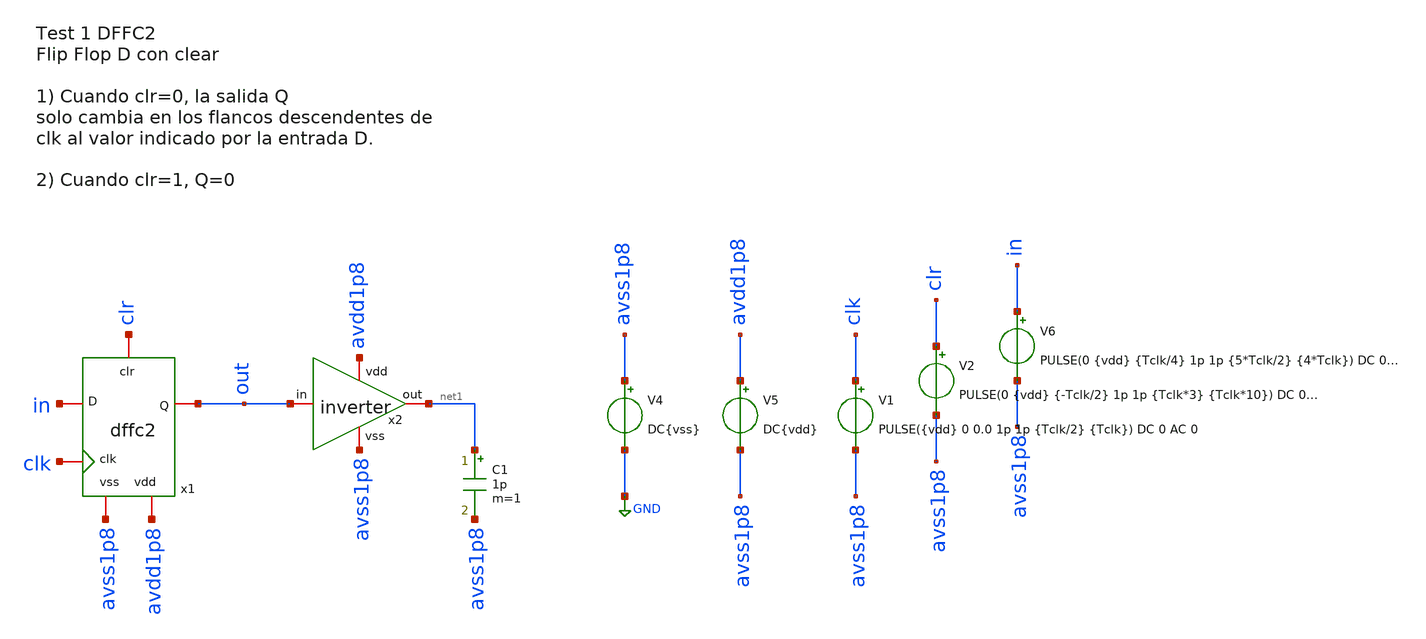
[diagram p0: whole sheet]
** sch_path: designs/sch/tests/test1_dffc2.sch
**.subckt test1_dffc2
x2 avdd1p8 net1 out avss1p8 inverter
V4 avss1p8 GND DC{vss}
V5 avdd1p8 avss1p8 DC{vdd}
V6 in avss1p8 PULSE(0 {vdd} {Tclk/4} 1p 1p {5*Tclk/2} {4*Tclk}) DC 0 AC 0
C1 net1 avss1p8 1p m=1
V1 clk avss1p8 PULSE({vdd} 0 0.0 1p 1p {Tclk/2} {Tclk}) DC 0 AC 0
V2 clr avss1p8 PULSE(0 {vdd} {-Tclk/2} 1p 1p {Tclk*3} {Tclk*10}) DC 0 AC 0
x1 out in clk clr avss1p8 avdd1p8 dffc2
**** begin user architecture code


* Circuit Parameters
.param vdd = 1.8
.param vss = 0.0
.param Tclk = 10n
.options TEMP = 65.0

* Include Models
.lib /foss/pdks/sky130A/libs.tech/ngspice/sky130.lib.spice TT

* OP Parameters & Singals to save
.save all

* Simulations
.control
  tran 0.01u 240n
  setplot tran1
  plot clr v(in)+2 v(out)+4 clk+6
reset
.endc

.end


**** end user architecture code
**.ends

* expanding   symbol:  /foss/designs/sch/inverter.sym # of pins=4
** sym_path: designs/inverter.sym
** sch_path: designs/inverter.sch
.subckt inverter vdd out in vss
*.iopin out
*.iopin vss
*.iopin vdd
*.iopin in
XM2 out in vss vss sky130_fd_pr__nfet_01v8 L=0.15 W=0.75 nf=1 ad='int((nf+1)/2) * W/nf * 0.29' as='int((nf+2)/2) * W/nf * 0.29'
+ pd='2*int((nf+1)/2) * (W/nf + 0.29)' ps='2*int((nf+2)/2) * (W/nf + 0.29)' nrd='0.29 / W' nrs='0.29 / W'
+ sa=0 sb=0 sd=0 mult=1 m=1
XM1 out in vdd vdd sky130_fd_pr__pfet_01v8 L=0.15 W=1.5 nf=1 ad='int((nf+1)/2) * W/nf * 0.29' as='int((nf+2)/2) * W/nf * 0.29'
+ pd='2*int((nf+1)/2) * (W/nf + 0.29)' ps='2*int((nf+2)/2) * (W/nf + 0.29)' nrd='0.29 / W' nrs='0.29 / W'
+ sa=0 sb=0 sd=0 mult=1 m=1
.ends


* expanding   symbol:  /foss/designs/sch/dffc2.sym # of pins=6
** sym_path: designs/dffc2.sym
** sch_path: designs/dffc2.sch
.subckt dffc2 Q D clk clr vss vdd
*.iopin clk
*.iopin clr
*.iopin vss
*.iopin vdd
*.iopin D
*.iopin Q
x1 vdd n_clk_2 clk_2 vss inverter
x2 vdd net4 net1 vss inverter
x3 vdd Qb Q vss inverter
x4 D n_clk_1 p_clk_1 net1 tg
x8 vdd Q clr net3 vss nor
x9 vdd net2 clr net4 vss nor
x5 net2 n_clk_2 p_clk_2 net1 tg
x6 net4 n_clk_2 p_clk_2 net3 tg
x7 Qb n_clk_1 p_clk_1 net3 tg
x10 vdd p_clk_2 n_clk_2 vss inverter
x11 clk_1 vss clk vdd clk_2 clockgen
x12 vdd n_clk_1 clk_1 vss inverter
x13 vdd p_clk_1 n_clk_1 vss inverter
.ends


* expanding   symbol:  /foss/designs/tg.sym # of pins=4
** sym_path: designs/tg.sym
** sch_path: designs/tg.sch
.subckt tg vin enb en vout
*.iopin vin
*.iopin vout
*.iopin enb
*.iopin en
XM1 vin en vout enb sky130_fd_pr__nfet_01v8 L=0.15 W=0.75 nf=1 ad='int((nf+1)/2) * W/nf * 0.29' as='int((nf+2)/2) * W/nf * 0.29'
+ pd='2*int((nf+1)/2) * (W/nf + 0.29)' ps='2*int((nf+2)/2) * (W/nf + 0.29)' nrd='0.29 / W' nrs='0.29 / W'
+ sa=0 sb=0 sd=0 mult=1 m=1
XM2 vout enb vin en sky130_fd_pr__pfet_01v8 L=0.15 W=1.5 nf=1 ad='int((nf+1)/2) * W/nf * 0.29' as='int((nf+2)/2) * W/nf * 0.29'
+ pd='2*int((nf+1)/2) * (W/nf + 0.29)' ps='2*int((nf+2)/2) * (W/nf + 0.29)' nrd='0.29 / W' nrs='0.29 / W'
+ sa=0 sb=0 sd=0 mult=1 m=1
.ends


* expanding   symbol:  /foss/designs/nor.sym # of pins=5
** sym_path: designs/sch/nor.sym
** sch_path: designs/sch/nor.sch
.subckt nor vdd Z A B vss
*.iopin A
*.iopin B
*.iopin vdd
*.iopin Z
*.iopin vss
XM1 Z A vss vss sky130_fd_pr__nfet_01v8 L=0.15 W=0.75 nf=1 ad='int((nf+1)/2) * W/nf * 0.29' as='int((nf+2)/2) * W/nf * 0.29'
+ pd='2*int((nf+1)/2) * (W/nf + 0.29)' ps='2*int((nf+2)/2) * (W/nf + 0.29)' nrd='0.29 / W' nrs='0.29 / W'
+ sa=0 sb=0 sd=0 mult=1 m=1
XM4 net1 B vdd vdd sky130_fd_pr__pfet_01v8 L=0.15 W=3 nf=1 ad='int((nf+1)/2) * W/nf * 0.29' as='int((nf+2)/2) * W/nf * 0.29'
+ pd='2*int((nf+1)/2) * (W/nf + 0.29)' ps='2*int((nf+2)/2) * (W/nf + 0.29)' nrd='0.29 / W' nrs='0.29 / W'
+ sa=0 sb=0 sd=0 mult=1 m=1
XM2 Z B vss vss sky130_fd_pr__nfet_01v8 L=0.15 W=0.75 nf=1 ad='int((nf+1)/2) * W/nf * 0.29' as='int((nf+2)/2) * W/nf * 0.29'
+ pd='2*int((nf+1)/2) * (W/nf + 0.29)' ps='2*int((nf+2)/2) * (W/nf + 0.29)' nrd='0.29 / W' nrs='0.29 / W'
+ sa=0 sb=0 sd=0 mult=1 m=1
XM3 Z A net1 vdd sky130_fd_pr__pfet_01v8 L=0.15 W=3 nf=1 ad='int((nf+1)/2) * W/nf * 0.29' as='int((nf+2)/2) * W/nf * 0.29'
+ pd='2*int((nf+1)/2) * (W/nf + 0.29)' ps='2*int((nf+2)/2) * (W/nf + 0.29)' nrd='0.29 / W' nrs='0.29 / W'
+ sa=0 sb=0 sd=0 mult=1 m=1
.ends


* expanding   symbol:  /foss/designs/clockgen.sym # of pins=5
** sym_path: designs/sch/clockgen.sym
** sch_path: designs/sch/clockgen.sch
.subckt clockgen clk1 vss clk vdd clk2
*.iopin vss
*.iopin vdd
*.iopin clk1
*.iopin clk2
*.iopin clk
x1 vdd net4 clk vss inverter
x2 vdd net2 net1 clk2 vss nor
x3 vdd net3 clk1 net4 vss nor
x4 vdd net7 clk vss inverter
x6 vdd net5 net2 vss inverter
x7 vdd net6 net3 vss inverter
x5 vdd clk1 net5 vss inverter
x8 vdd clk2 net6 vss inverter
x9 vdd net1 net7 vss inverter
.ends

.GLOBAL GND
.end
